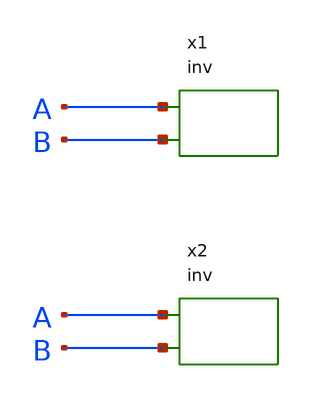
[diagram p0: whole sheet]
** sch_path: tests/golden/SCHEM/cases/SCHEM-NL-16/input/nl16.sch
**.subckt nl16
x1 A B inv
x2 A B inv
**.ends

* expanding   symbol:  libA/inv.sym # of pins=2
** sym_path: tests/golden/SCHEM/cases/SCHEM-NL-20/input/with/inv.sym
** sch_path: tests/golden/SCHEM/cases/SCHEM-NL-20/input/with/inv.sch
.subckt inv A Y
*.opin Y
*.ipin A
R1 Y A 1k m=1
.ends

.end
